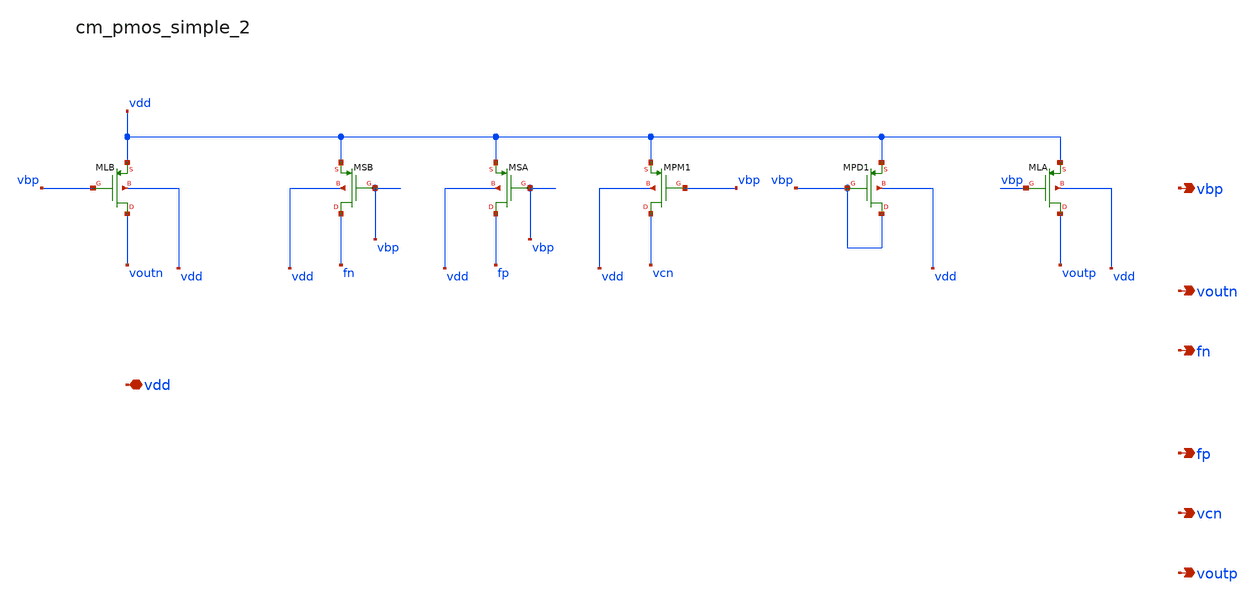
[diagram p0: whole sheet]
** sch_path: analog-db/raw/amp_023_fer_fd2s/hier/blocks/cm_pmos_simple_2.sch
**.subckt cm_pmos_simple_2 vdd vbp voutn fn fp vcn voutp
*.iopin vdd
*.opin vbp
*.opin voutn
*.opin fn
*.opin fp
*.opin vcn
*.opin voutp
XMLA voutp vbp vdd vdd sg13_lv_pmos w=x_dut_xmla_w l=x_dut_xmla_l ng=1 m=x_dut_xmla_m
XMLB voutn vbp vdd vdd sg13_lv_pmos w=x_dut_xmlb_w l=x_dut_xmlb_l ng=1 m=x_dut_xmlb_m
XMPD1 vbp vbp vdd vdd sg13_lv_pmos w=x_dut_xmpd1_w l=x_dut_xmpd1_l ng=1 m=x_dut_xmpd1_m
XMPM1 vcn vbp vdd vdd sg13_lv_pmos w=x_dut_xmpm1_w l=x_dut_xmpm1_l ng=1 m=x_dut_xmpm1_m
XMSA fp vbp vdd vdd sg13_lv_pmos w=x_dut_xmsa_w l=x_dut_xmsa_l ng=1 m=x_dut_xmsa_m
XMSB fn vbp vdd vdd sg13_lv_pmos w=x_dut_xmsb_w l=x_dut_xmsb_l ng=1 m=x_dut_xmsb_m
**.ends
.end
